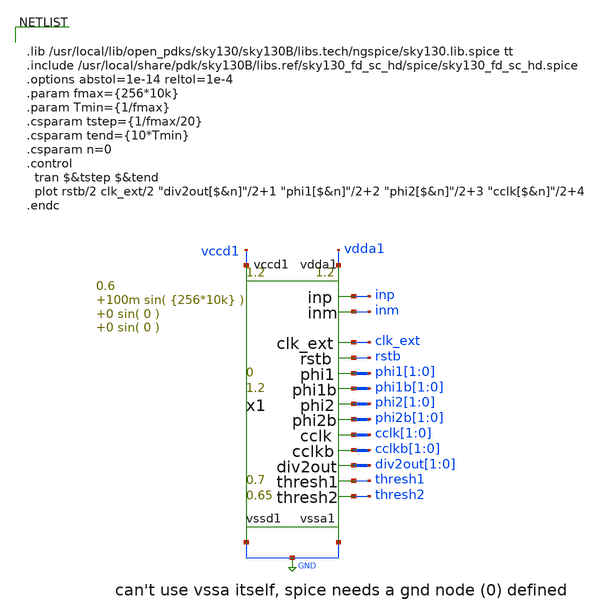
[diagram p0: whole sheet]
** sch_path: xschem/test_bench/risc_signals_tb.sch
**.subckt risc_signals_tb
x1 thresh1 thresh2 vdda1 GND inp inm clk_ext rstb vccd1 GND phi1[1] phi1[0] phi1b[1] phi1b[0] phi2[1]
+ phi2[0] phi2b[1] phi2b[0] cclk[1] cclk[0] cclkb[1] cclkb[0] div2out[1] div2out[0] risc_signals p_vdda1=1.2
+ p_vccd1=1.2 p_fclk={256*10k} p_duty_cycle=0.5 p_rstb_delay={1.5/p_fclk} p_rstb_tr=5n p_thresh1=0.7 p_thresh2=0.65
+ p_vpb=0 p_vnb=1.2 p_vcm=0.6 p_amp1=100m p_f1={256*10k} p_amp2=0 p_f2=0 p_amp3=0 p_f3=0
**** begin user architecture code


.lib /usr/local/lib/open_pdks/sky130/sky130B/libs.tech/ngspice/sky130.lib.spice tt
.include /usr/local/share/pdk/sky130B/libs.ref/sky130_fd_sc_hd/spice/sky130_fd_sc_hd.spice
.options abstol=1e-14 reltol=1e-4
.param fmax={256*10k}
.param Tmin={1/fmax}
.csparam tstep={1/fmax/20}
.csparam tend={10*Tmin}
.csparam n=0
.control
  tran $&tstep $&tend
  plot rstb/2 clk_ext/2 "div2out[$&n]"/2+1 "phi1[$&n]"/2+2 "phi2[$&n]"/2+3 "cclk[$&n]"/2+4
.endc


**** end user architecture code
**.ends
.GLOBAL GND
.end
